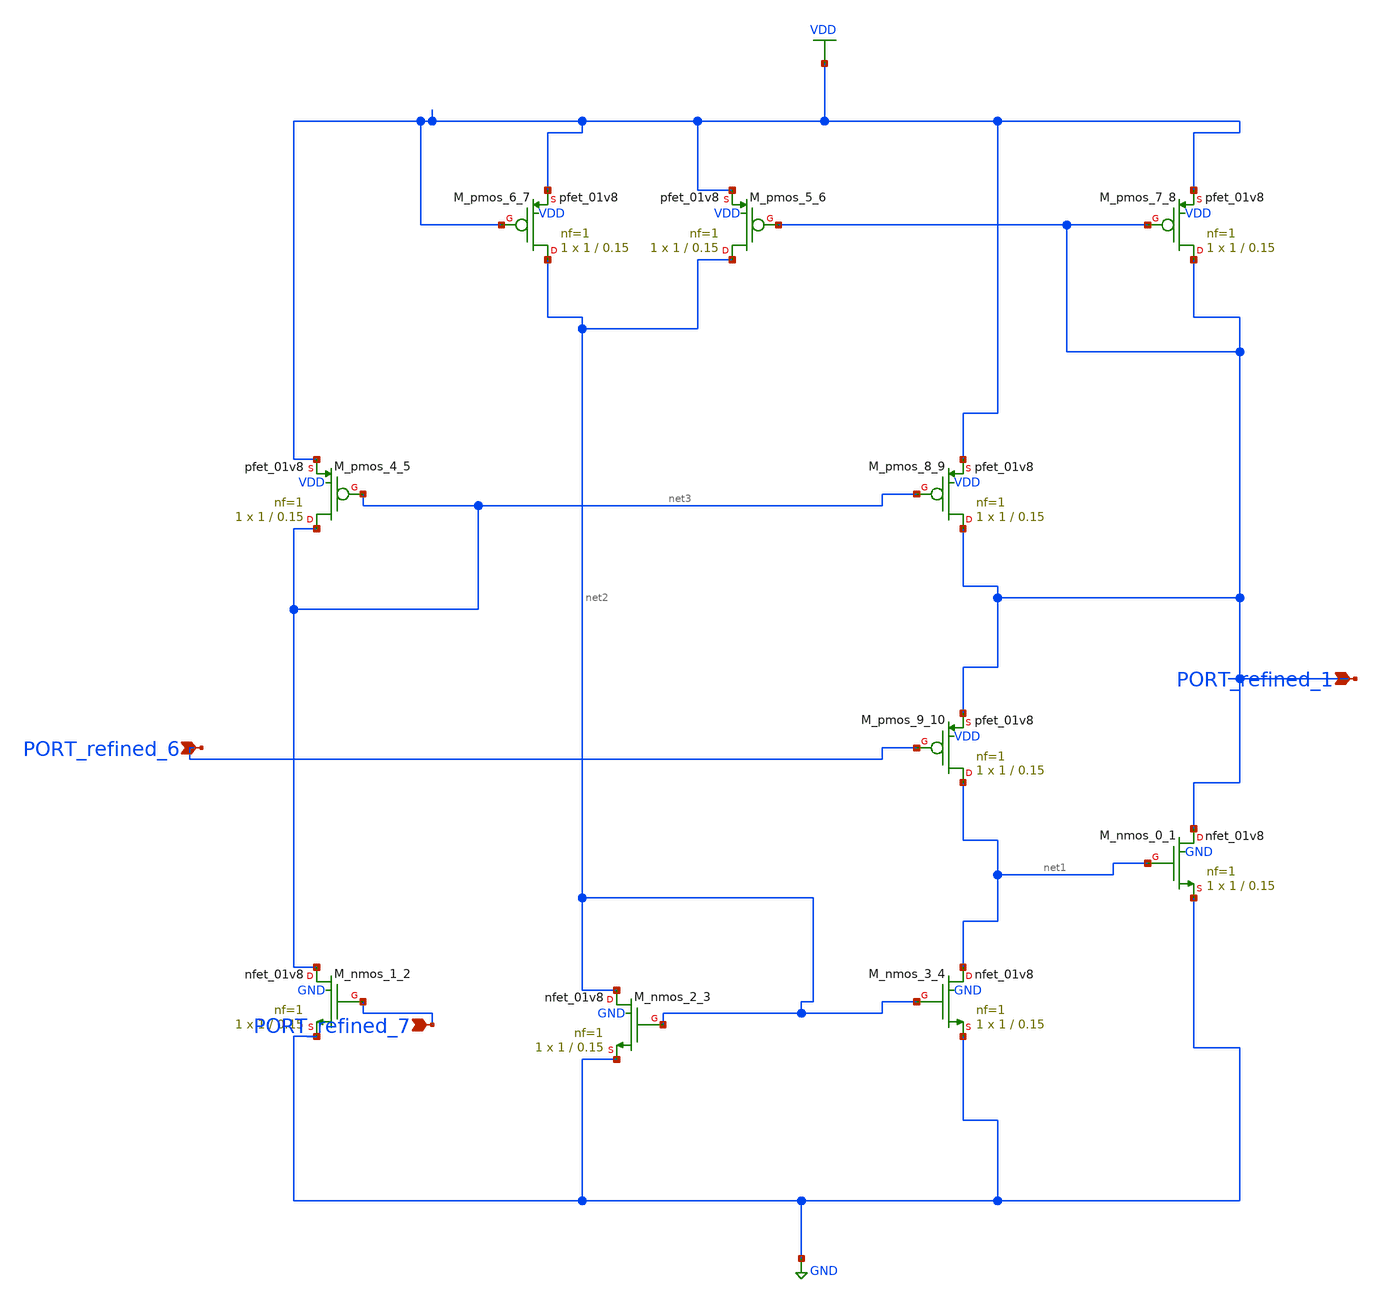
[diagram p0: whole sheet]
** sch_path: schematics/SchemGen/10_1587_elex_XX_XXXXXXXX_03_002.sch
**.subckt 10_1587_elex_XX_XXXXXXXX_03_002 PORT_refined_1 PORT_refined_6 PORT_refined_7
*.ipin PORT_refined_1
*.ipin PORT_refined_6
*.ipin PORT_refined_7
XM_nmos_0_1 PORT_refined_1 net1 GND GND sky130_fd_pr__nfet_01v8 L=0.15 W=1 nf=1 ad='int((1 + 1)/2) * 1 / 1 * 0.29'
+ as='int((1 + 2)/2) * 1 / 1 * 0.29' pd='2*int((1 + 1)/2) * (1 / 1 + 0.29)' ps='2*int((1 + 2)/2) * (1 / 1 + 0.29)'
+ nrd='0.29 / 1 ' nrs='0.29 / 1 ' sa=0 sb=0 sd=0 mult=1 m=1
XM_nmos_1_2 net3 PORT_refined_7 GND GND sky130_fd_pr__nfet_01v8 L=0.15 W=1 nf=1 ad='int((1 + 1)/2) * 1 / 1 * 0.29'
+ as='int((1 + 2)/2) * 1 / 1 * 0.29' pd='2*int((1 + 1)/2) * (1 / 1 + 0.29)' ps='2*int((1 + 2)/2) * (1 / 1 + 0.29)'
+ nrd='0.29 / 1 ' nrs='0.29 / 1 ' sa=0 sb=0 sd=0 mult=1 m=1
XM_nmos_2_3 net2 net2 GND GND sky130_fd_pr__nfet_01v8 L=0.15 W=1 nf=1 ad='int((1 + 1)/2) * 1 / 1 * 0.29'
+ as='int((1 + 2)/2) * 1 / 1 * 0.29' pd='2*int((1 + 1)/2) * (1 / 1 + 0.29)' ps='2*int((1 + 2)/2) * (1 / 1 + 0.29)'
+ nrd='0.29 / 1 ' nrs='0.29 / 1 ' sa=0 sb=0 sd=0 mult=1 m=1
XM_nmos_3_4 net1 net2 GND GND sky130_fd_pr__nfet_01v8 L=0.15 W=1 nf=1 ad='int((1 + 1)/2) * 1 / 1 * 0.29'
+ as='int((1 + 2)/2) * 1 / 1 * 0.29' pd='2*int((1 + 1)/2) * (1 / 1 + 0.29)' ps='2*int((1 + 2)/2) * (1 / 1 + 0.29)'
+ nrd='0.29 / 1 ' nrs='0.29 / 1 ' sa=0 sb=0 sd=0 mult=1 m=1
XM_pmos_4_5 net3 net3 VDD VDD sky130_fd_pr__pfet_01v8 L=0.15 W=1 nf=1 ad='int((1 + 1)/2) * 1 / 1 * 0.29'
+ as='int((1 + 2)/2) * 1 / 1 * 0.29' pd='2*int((1 + 1)/2) * (1 / 1 + 0.29)' ps='2*int((1 + 2)/2) * (1 / 1 + 0.29)'
+ nrd='0.29 / 1 ' nrs='0.29 / 1 ' sa=0 sb=0 sd=0 mult=1 m=1
XM_pmos_5_6 net2 PORT_refined_1 VDD VDD sky130_fd_pr__pfet_01v8 L=0.15 W=1 nf=1 ad='int((1 + 1)/2) * 1 / 1 * 0.29'
+ as='int((1 + 2)/2) * 1 / 1 * 0.29' pd='2*int((1 + 1)/2) * (1 / 1 + 0.29)' ps='2*int((1 + 2)/2) * (1 / 1 + 0.29)'
+ nrd='0.29 / 1 ' nrs='0.29 / 1 ' sa=0 sb=0 sd=0 mult=1 m=1
XM_pmos_6_7 net2 VDD VDD VDD sky130_fd_pr__pfet_01v8 L=0.15 W=1 nf=1 ad='int((1 + 1)/2) * 1 / 1 * 0.29'
+ as='int((1 + 2)/2) * 1 / 1 * 0.29' pd='2*int((1 + 1)/2) * (1 / 1 + 0.29)' ps='2*int((1 + 2)/2) * (1 / 1 + 0.29)'
+ nrd='0.29 / 1 ' nrs='0.29 / 1 ' sa=0 sb=0 sd=0 mult=1 m=1
XM_pmos_7_8 PORT_refined_1 PORT_refined_1 VDD VDD sky130_fd_pr__pfet_01v8 L=0.15 W=1 nf=1 ad='int((1 + 1)/2) * 1 / 1 * 0.29'
+ as='int((1 + 2)/2) * 1 / 1 * 0.29' pd='2*int((1 + 1)/2) * (1 / 1 + 0.29)' ps='2*int((1 + 2)/2) * (1 / 1 + 0.29)'
+ nrd='0.29 / 1 ' nrs='0.29 / 1 ' sa=0 sb=0 sd=0 mult=1 m=1
XM_pmos_8_9 PORT_refined_1 net3 VDD VDD sky130_fd_pr__pfet_01v8 L=0.15 W=1 nf=1 ad='int((1 + 1)/2) * 1 / 1 * 0.29'
+ as='int((1 + 2)/2) * 1 / 1 * 0.29' pd='2*int((1 + 1)/2) * (1 / 1 + 0.29)' ps='2*int((1 + 2)/2) * (1 / 1 + 0.29)'
+ nrd='0.29 / 1 ' nrs='0.29 / 1 ' sa=0 sb=0 sd=0 mult=1 m=1
XM_pmos_9_10 net1 PORT_refined_6 PORT_refined_1 VDD sky130_fd_pr__pfet_01v8 L=0.15 W=1 nf=1 ad='int((1 + 1)/2) * 1 / 1 * 0.29'
+ as='int((1 + 2)/2) * 1 / 1 * 0.29' pd='2*int((1 + 1)/2) * (1 / 1 + 0.29)' ps='2*int((1 + 2)/2) * (1 / 1 + 0.29)'
+ nrd='0.29 / 1 ' nrs='0.29 / 1 ' sa=0 sb=0 sd=0 mult=1 m=1
**.ends
.GLOBAL GND
.GLOBAL VDD
.end
